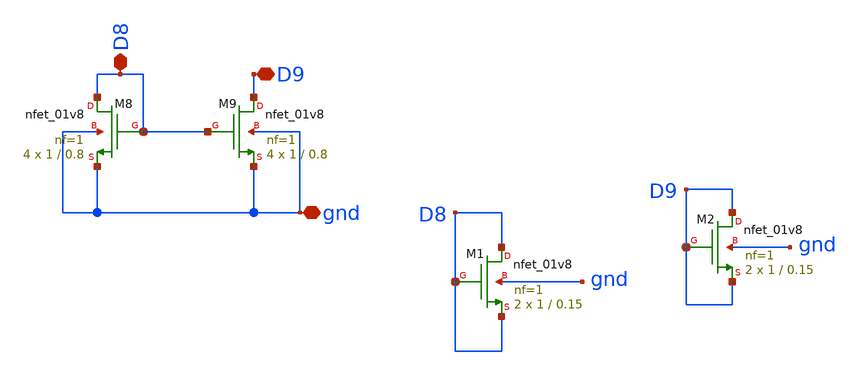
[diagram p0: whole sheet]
** sch_path: opamp/mag/nmoscss.sch
**.subckt nmoscss gnd D9 D8
*.iopin gnd
*.iopin D9
*.iopin D8
XM8 D8 D8 gnd gnd sky130_fd_pr__nfet_01v8 L=0.8 W=1 nf=1 ad='int((nf+1)/2) * W/nf * 0.29' as='int((nf+2)/2) * W/nf * 0.29'
+ pd='2*int((nf+1)/2) * (W/nf + 0.29)' ps='2*int((nf+2)/2) * (W/nf + 0.29)' nrd='0.29 / W' nrs='0.29 / W'
+ sa=0 sb=0 sd=0 mult=4 m=4
XM9 D9 D8 gnd gnd sky130_fd_pr__nfet_01v8 L=0.8 W=1 nf=1 ad='int((nf+1)/2) * W/nf * 0.29' as='int((nf+2)/2) * W/nf * 0.29'
+ pd='2*int((nf+1)/2) * (W/nf + 0.29)' ps='2*int((nf+2)/2) * (W/nf + 0.29)' nrd='0.29 / W' nrs='0.29 / W'
+ sa=0 sb=0 sd=0 mult=4 m=4
XM1 D8 D8 D8 gnd sky130_fd_pr__nfet_01v8 L=0.15 W=1 nf=1 ad='int((nf+1)/2) * W/nf * 0.29' as='int((nf+2)/2) * W/nf * 0.29'
+ pd='2*int((nf+1)/2) * (W/nf + 0.29)' ps='2*int((nf+2)/2) * (W/nf + 0.29)' nrd='0.29 / W' nrs='0.29 / W'
+ sa=0 sb=0 sd=0 mult=2 m=2
XM2 D9 D9 D9 gnd sky130_fd_pr__nfet_01v8 L=0.15 W=1 nf=1 ad='int((nf+1)/2) * W/nf * 0.29' as='int((nf+2)/2) * W/nf * 0.29'
+ pd='2*int((nf+1)/2) * (W/nf + 0.29)' ps='2*int((nf+2)/2) * (W/nf + 0.29)' nrd='0.29 / W' nrs='0.29 / W'
+ sa=0 sb=0 sd=0 mult=2 m=2
**.ends
.end
